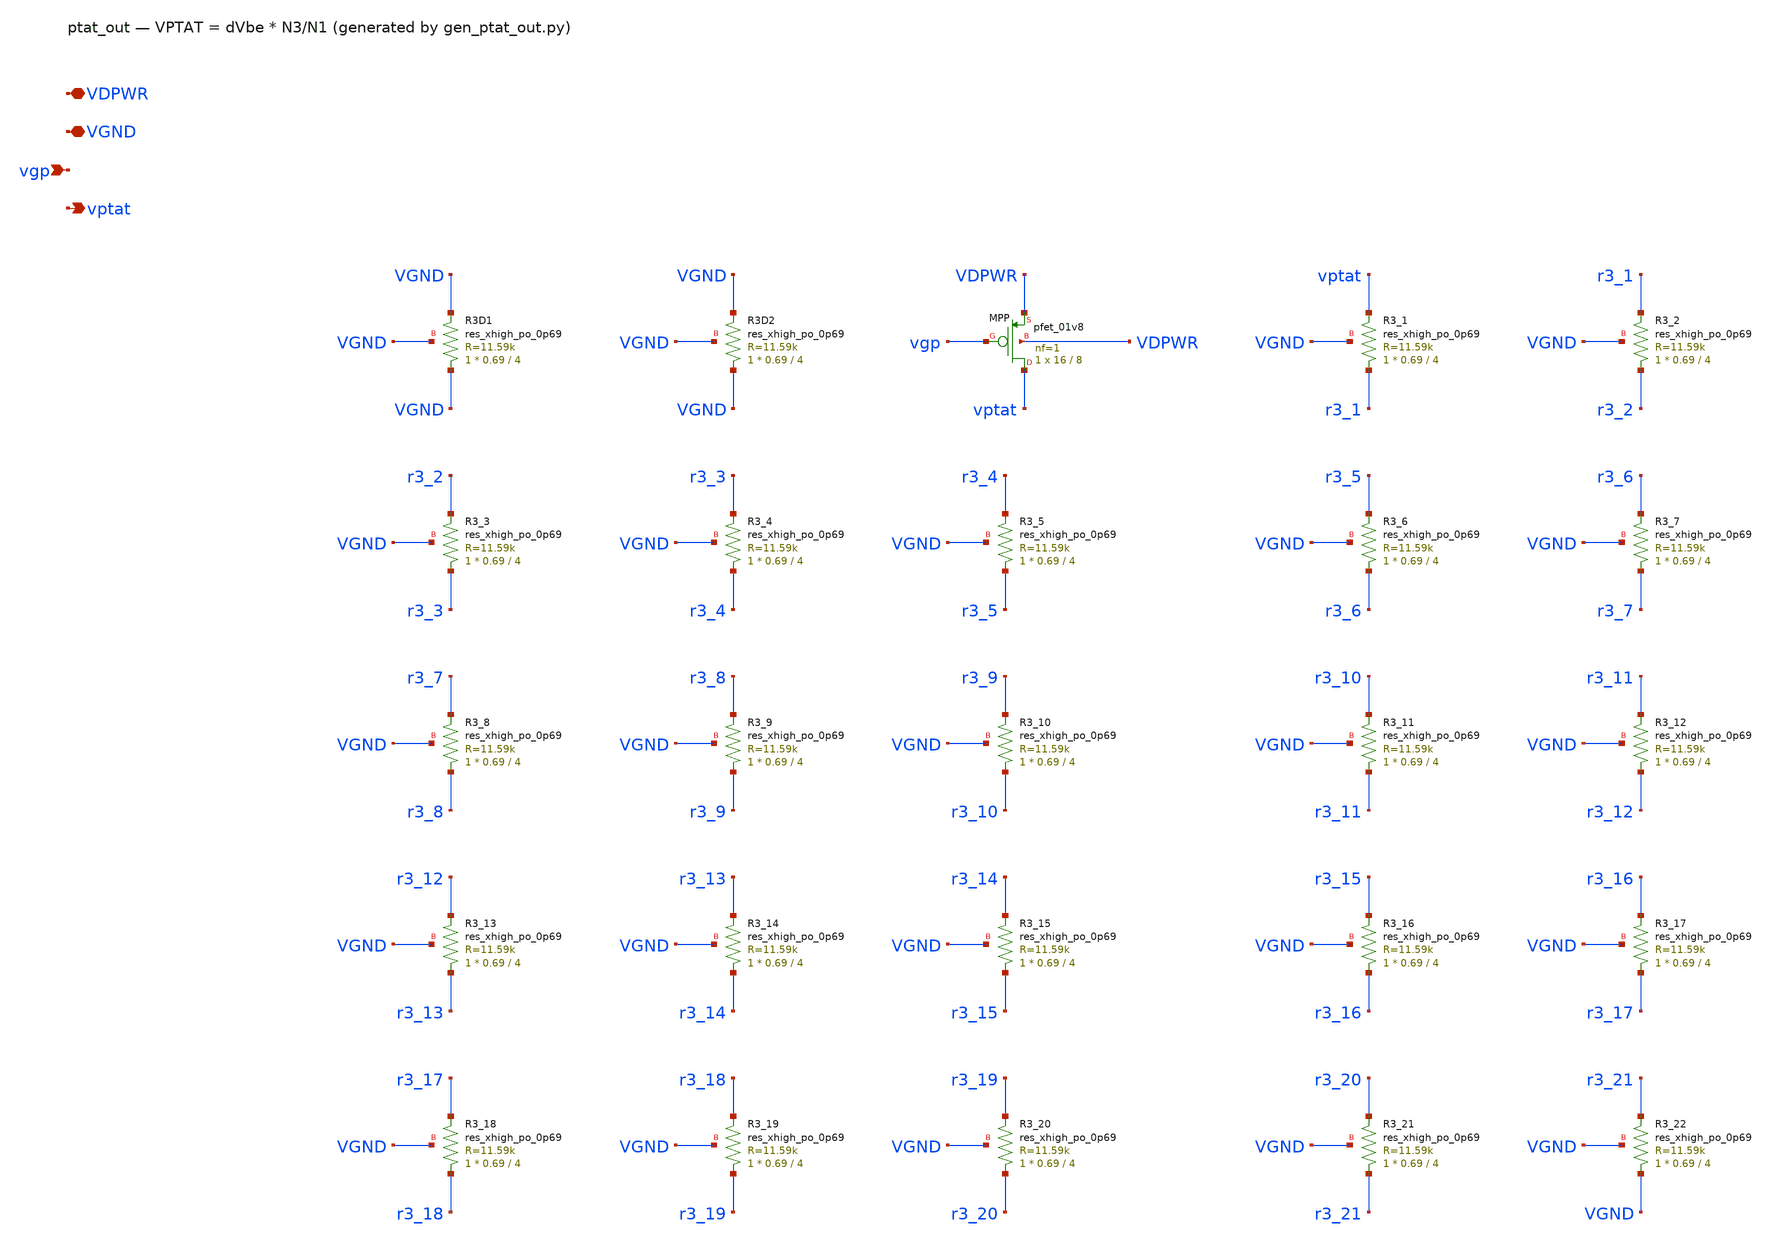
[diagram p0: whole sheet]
** sch_path: xschem/ptat_out.sch
**.subckt ptat_out VDPWR VGND vgp vptat
*.iopin VDPWR
*.iopin VGND
*.ipin vgp
*.opin vptat
XR3D1 VGND VGND VGND sky130_fd_pr__res_xhigh_po_0p69 L=4 mult=1 m=1
XR3D2 VGND VGND VGND sky130_fd_pr__res_xhigh_po_0p69 L=4 mult=1 m=1
XMPP vptat vgp VDPWR VDPWR sky130_fd_pr__pfet_01v8 L=8 W=16 nf=1 ad='int((nf+1)/2) * W/nf * 0.29' as='int((nf+2)/2) * W/nf * 0.29'
+ pd='2*int((nf+1)/2) * (W/nf + 0.29)' ps='2*int((nf+2)/2) * (W/nf + 0.29)' nrd='0.29 / W' nrs='0.29 / W'
+ sa=0 sb=0 sd=0 mult=1 m=1
XR3_1 r3_1 vptat VGND sky130_fd_pr__res_xhigh_po_0p69 L=4 mult=1 m=1
XR3_2 r3_2 r3_1 VGND sky130_fd_pr__res_xhigh_po_0p69 L=4 mult=1 m=1
XR3_3 r3_3 r3_2 VGND sky130_fd_pr__res_xhigh_po_0p69 L=4 mult=1 m=1
XR3_4 r3_4 r3_3 VGND sky130_fd_pr__res_xhigh_po_0p69 L=4 mult=1 m=1
XR3_5 r3_5 r3_4 VGND sky130_fd_pr__res_xhigh_po_0p69 L=4 mult=1 m=1
XR3_6 r3_6 r3_5 VGND sky130_fd_pr__res_xhigh_po_0p69 L=4 mult=1 m=1
XR3_7 r3_7 r3_6 VGND sky130_fd_pr__res_xhigh_po_0p69 L=4 mult=1 m=1
XR3_8 r3_8 r3_7 VGND sky130_fd_pr__res_xhigh_po_0p69 L=4 mult=1 m=1
XR3_9 r3_9 r3_8 VGND sky130_fd_pr__res_xhigh_po_0p69 L=4 mult=1 m=1
XR3_10 r3_10 r3_9 VGND sky130_fd_pr__res_xhigh_po_0p69 L=4 mult=1 m=1
XR3_11 r3_11 r3_10 VGND sky130_fd_pr__res_xhigh_po_0p69 L=4 mult=1 m=1
XR3_12 r3_12 r3_11 VGND sky130_fd_pr__res_xhigh_po_0p69 L=4 mult=1 m=1
XR3_13 r3_13 r3_12 VGND sky130_fd_pr__res_xhigh_po_0p69 L=4 mult=1 m=1
XR3_14 r3_14 r3_13 VGND sky130_fd_pr__res_xhigh_po_0p69 L=4 mult=1 m=1
XR3_15 r3_15 r3_14 VGND sky130_fd_pr__res_xhigh_po_0p69 L=4 mult=1 m=1
XR3_16 r3_16 r3_15 VGND sky130_fd_pr__res_xhigh_po_0p69 L=4 mult=1 m=1
XR3_17 r3_17 r3_16 VGND sky130_fd_pr__res_xhigh_po_0p69 L=4 mult=1 m=1
XR3_18 r3_18 r3_17 VGND sky130_fd_pr__res_xhigh_po_0p69 L=4 mult=1 m=1
XR3_19 r3_19 r3_18 VGND sky130_fd_pr__res_xhigh_po_0p69 L=4 mult=1 m=1
XR3_20 r3_20 r3_19 VGND sky130_fd_pr__res_xhigh_po_0p69 L=4 mult=1 m=1
XR3_21 r3_21 r3_20 VGND sky130_fd_pr__res_xhigh_po_0p69 L=4 mult=1 m=1
XR3_22 VGND r3_21 VGND sky130_fd_pr__res_xhigh_po_0p69 L=4 mult=1 m=1
**.ends
.end
